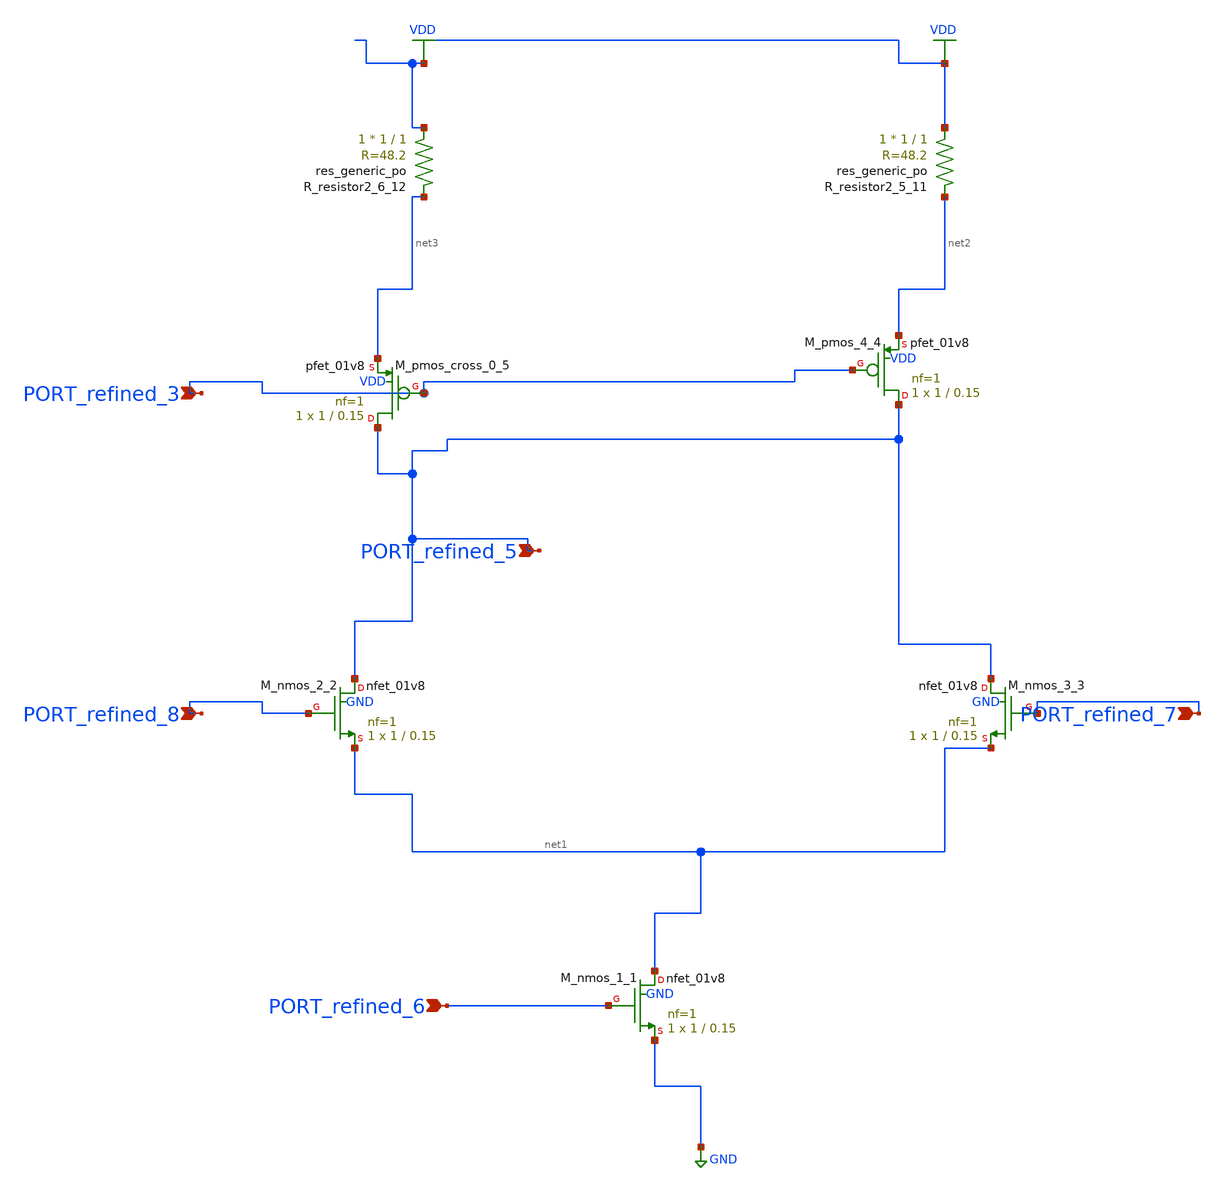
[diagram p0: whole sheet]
** sch_path: schematics/AMSNet/238.sch
**.subckt 238 PORT_refined_3 PORT_refined_6 PORT_refined_7 PORT_refined_8 PORT_refined_5
*.ipin PORT_refined_3
*.ipin PORT_refined_6
*.ipin PORT_refined_7
*.ipin PORT_refined_8
*.ipin PORT_refined_5
XM_nmos_1_1 net1 PORT_refined_6 GND GND sky130_fd_pr__nfet_01v8 L=0.15 W=1 nf=1 ad='int((1 + 1)/2) * 1 / 1 * 0.29'
+ as='int((1 + 2)/2) * 1 / 1 * 0.29' pd='2*int((1 + 1)/2) * (1 / 1 + 0.29)' ps='2*int((1 + 2)/2) * (1 / 1 + 0.29)'
+ nrd='0.29 / 1 ' nrs='0.29 / 1 ' sa=0 sb=0 sd=0 mult=1 m=1
XM_nmos_2_2 PORT_refined_5 PORT_refined_8 net1 GND sky130_fd_pr__nfet_01v8 L=0.15 W=1 nf=1 ad='int((1 + 1)/2) * 1 / 1 * 0.29'
+ as='int((1 + 2)/2) * 1 / 1 * 0.29' pd='2*int((1 + 1)/2) * (1 / 1 + 0.29)' ps='2*int((1 + 2)/2) * (1 / 1 + 0.29)'
+ nrd='0.29 / 1 ' nrs='0.29 / 1 ' sa=0 sb=0 sd=0 mult=1 m=1
XM_nmos_3_3 PORT_refined_5 PORT_refined_7 net1 GND sky130_fd_pr__nfet_01v8 L=0.15 W=1 nf=1 ad='int((1 + 1)/2) * 1 / 1 * 0.29'
+ as='int((1 + 2)/2) * 1 / 1 * 0.29' pd='2*int((1 + 1)/2) * (1 / 1 + 0.29)' ps='2*int((1 + 2)/2) * (1 / 1 + 0.29)'
+ nrd='0.29 / 1 ' nrs='0.29 / 1 ' sa=0 sb=0 sd=0 mult=1 m=1
XM_pmos_4_4 PORT_refined_5 PORT_refined_3 net2 VDD sky130_fd_pr__pfet_01v8 L=0.15 W=1 nf=1 ad='int((1 + 1)/2) * 1 / 1 * 0.29'
+ as='int((1 + 2)/2) * 1 / 1 * 0.29' pd='2*int((1 + 1)/2) * (1 / 1 + 0.29)' ps='2*int((1 + 2)/2) * (1 / 1 + 0.29)'
+ nrd='0.29 / 1 ' nrs='0.29 / 1 ' sa=0 sb=0 sd=0 mult=1 m=1
XM_pmos_cross_0_5 PORT_refined_5 PORT_refined_3 net3 VDD sky130_fd_pr__pfet_01v8 L=0.15 W=1 nf=1 ad='int((1 + 1)/2) * 1 / 1 * 0.29'
+ as='int((1 + 2)/2) * 1 / 1 * 0.29' pd='2*int((1 + 1)/2) * (1 / 1 + 0.29)' ps='2*int((1 + 2)/2) * (1 / 1 + 0.29)'
+ nrd='0.29 / 1 ' nrs='0.29 / 1 ' sa=0 sb=0 sd=0 mult=1 m=1
XR_resistor2_5_11 VDD net2 sky130_fd_pr__res_generic_po W=1 L=1 m=1
XR_resistor2_6_12 VDD net3 sky130_fd_pr__res_generic_po W=1 L=1 m=1
**.ends
.GLOBAL GND
.GLOBAL VDD
.end
